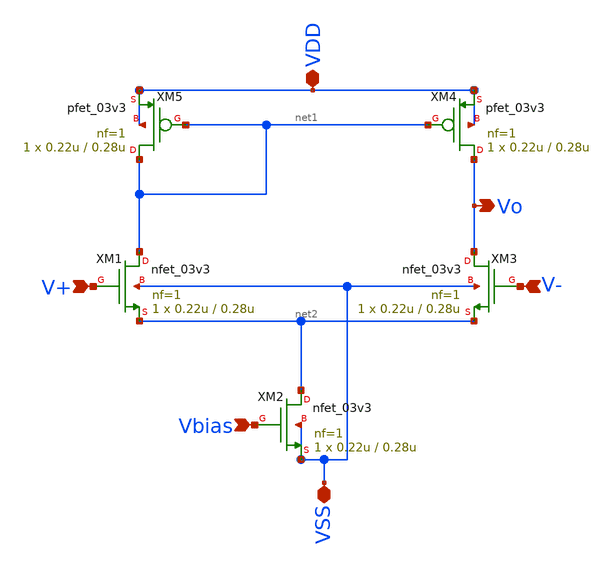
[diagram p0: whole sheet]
** sch_path: analog/diff_amp.sch
**.subckt diff_amp VDD VSS V+ V- Vo Vbias
*.iopin VDD
*.iopin VSS
*.ipin V+
*.ipin V-
*.opin Vo
*.ipin Vbias
XM1 net1 V+ net2 VSS nfet_03v3 L=0.28u W=0.22u nf=1 ad='int((nf+1)/2) * W/nf * 0.18u' as='int((nf+2)/2) * W/nf * 0.18u'
+ pd='2*int((nf+1)/2) * (W/nf + 0.18u)' ps='2*int((nf+2)/2) * (W/nf + 0.18u)' nrd='0.18u / W' nrs='0.18u / W'
+ sa=0 sb=0 sd=0 m=1
XM2 net2 Vbias VSS VSS nfet_03v3 L=0.28u W=0.22u nf=1 ad='int((nf+1)/2) * W/nf * 0.18u' as='int((nf+2)/2) * W/nf * 0.18u'
+ pd='2*int((nf+1)/2) * (W/nf + 0.18u)' ps='2*int((nf+2)/2) * (W/nf + 0.18u)' nrd='0.18u / W' nrs='0.18u / W'
+ sa=0 sb=0 sd=0 m=1
XM3 Vo V- net2 VSS nfet_03v3 L=0.28u W=0.22u nf=1 ad='int((nf+1)/2) * W/nf * 0.18u' as='int((nf+2)/2) * W/nf * 0.18u'
+ pd='2*int((nf+1)/2) * (W/nf + 0.18u)' ps='2*int((nf+2)/2) * (W/nf + 0.18u)' nrd='0.18u / W' nrs='0.18u / W'
+ sa=0 sb=0 sd=0 m=1
XM4 Vo net1 VDD VDD pfet_03v3 L=0.28u W=0.22u nf=1 ad='int((nf+1)/2) * W/nf * 0.18u' as='int((nf+2)/2) * W/nf * 0.18u'
+ pd='2*int((nf+1)/2) * (W/nf + 0.18u)' ps='2*int((nf+2)/2) * (W/nf + 0.18u)' nrd='0.18u / W' nrs='0.18u / W'
+ sa=0 sb=0 sd=0 m=1
XM5 net1 net1 VDD VDD pfet_03v3 L=0.28u W=0.22u nf=1 ad='int((nf+1)/2) * W/nf * 0.18u' as='int((nf+2)/2) * W/nf * 0.18u'
+ pd='2*int((nf+1)/2) * (W/nf + 0.18u)' ps='2*int((nf+2)/2) * (W/nf + 0.18u)' nrd='0.18u / W' nrs='0.18u / W'
+ sa=0 sb=0 sd=0 m=1
**.ends
.end
